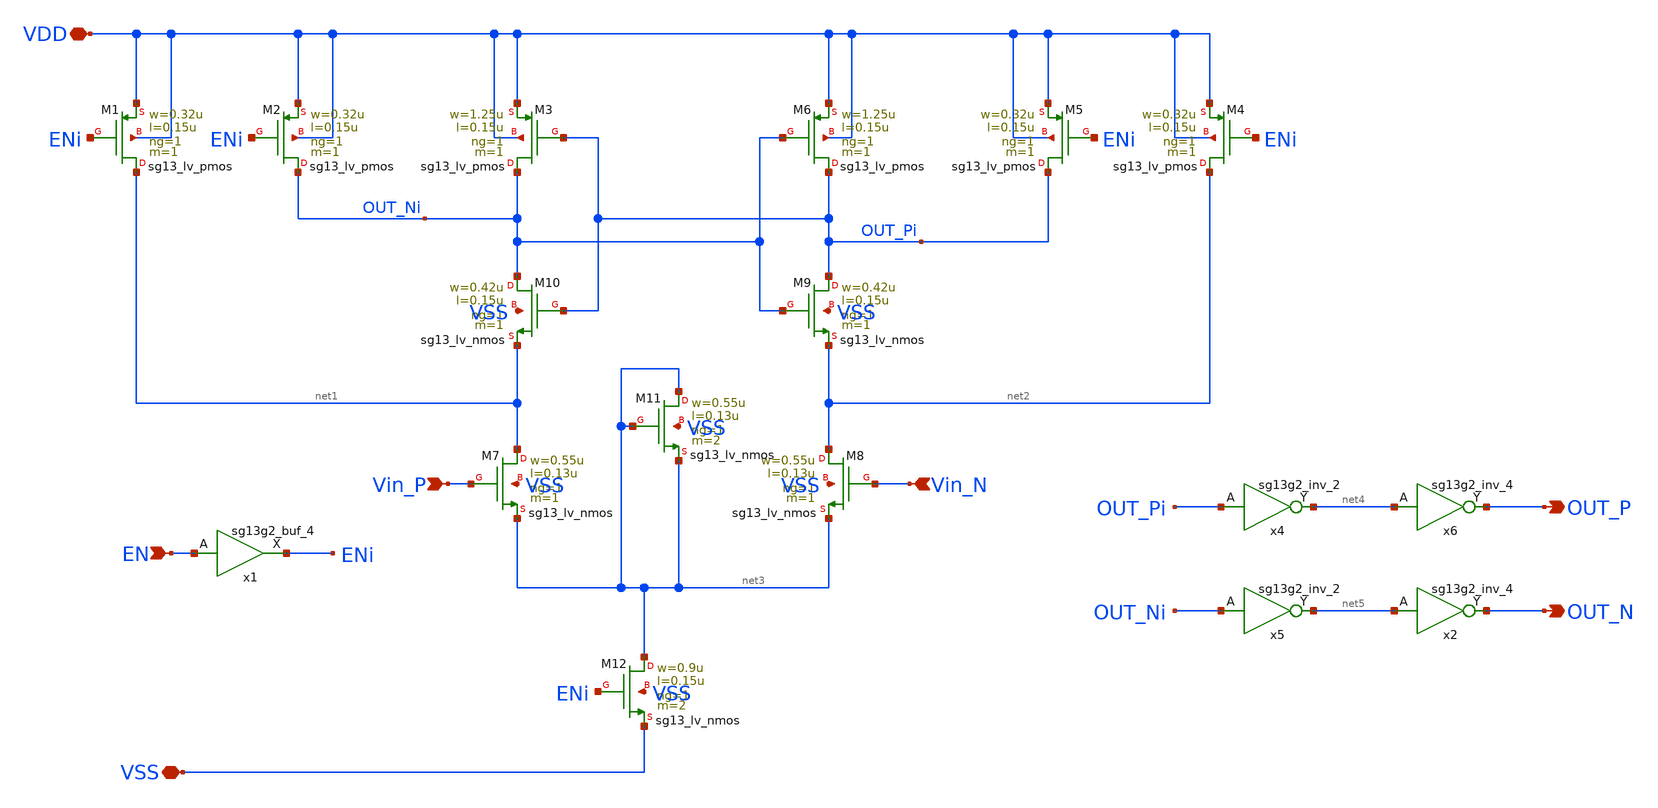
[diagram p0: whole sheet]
** sch_path: schematic/latched_comparator/latched_comparator.sch
* IHP-GmbH/IHP-Open-PDK/ihp-sg13g2/libs.tech/xschem/sg13g2_stdcells/sg13g2_buf_4.sch:
* Copyright 2023 IHP PDK Authors
* Licensed under the Apache License, Version 2.0 (the "License");
**.subckt latched_comparator Vin_P Vin_N VDD VSS EN OUT_P OUT_N
*.ipin Vin_P
*.ipin Vin_N
*.iopin VDD
*.iopin VSS
*.ipin EN
*.opin OUT_P
*.opin OUT_N
XM1 net1 ENi VDD VDD sg13_lv_pmos w=0.32u l=0.15u ng=1 m=1 mm_ok=1
XM2 OUT_Ni ENi VDD VDD sg13_lv_pmos w=0.32u l=0.15u ng=1 m=1 mm_ok=1
XM3 OUT_Ni OUT_Pi VDD VDD sg13_lv_pmos w=1.25u l=0.15u ng=1 m=1 mm_ok=1
XM4 net2 ENi VDD VDD sg13_lv_pmos w=0.32u l=0.15u ng=1 m=1 mm_ok=1
XM5 OUT_Pi ENi VDD VDD sg13_lv_pmos w=0.32u l=0.15u ng=1 m=1 mm_ok=1
XM6 OUT_Pi OUT_Ni VDD VDD sg13_lv_pmos w=1.25u l=0.15u ng=1 m=1 mm_ok=1
XM7 net1 Vin_P net3 VSS sg13_lv_nmos w=0.55u l=0.13u ng=1 m=1 mm_ok=1
XM8 net2 Vin_N net3 VSS sg13_lv_nmos w=0.55u l=0.13u ng=1 m=1 mm_ok=1
XM9 OUT_Pi OUT_Ni net2 VSS sg13_lv_nmos w=0.42u l=0.15u ng=1 m=1 mm_ok=1
XM10 OUT_Ni OUT_Pi net1 VSS sg13_lv_nmos w=0.42u l=0.15u ng=1 m=1 mm_ok=1
XM11 net3 net3 net3 VSS sg13_lv_nmos w=0.55u l=0.13u ng=1 m=2 mm_ok=1
XM12 net3 ENi VSS VSS sg13_lv_nmos w=0.9u l=0.15u ng=1 m=2 mm_ok=1
x4 net4 OUT_Pi VDD VSS sg13g2_inv_2
x5 net5 OUT_Ni VDD VSS sg13g2_inv_2
x1 ENi EN VDD VSS sg13g2_buf_4
x6 OUT_P net4 VDD VSS sg13g2_inv_4
x2 OUT_N net5 VDD VSS sg13g2_inv_4
**.ends

* expanding   symbol:  sg13g2_stdcells/sg13g2_inv_2.sym # of pins=2
** sym_path: sg13g2_stdcells/sg13g2_inv_2.sym
** sch_path: sg13g2_stdcells/sg13g2_inv_2.sch
.subckt sg13g2_inv_2 Y A VDD VSS
*.opin Y
*.ipin A
*.iopin VDD
*.iopin VSS
XM1 Y A VSS VSS sg13_lv_nmos w=1.48u l=130.00n ng=2 m=1 mm_ok=1
XM2 Y A VDD VDD sg13_lv_pmos w=2.24u l=130.00n ng=2 m=1 mm_ok=1
.ends


* expanding   symbol:  sg13g2_stdcells/sg13g2_buf_4.sym # of pins=2
** sym_path: sg13g2_stdcells/sg13g2_buf_4.sym
** sch_path: sg13g2_stdcells/sg13g2_buf_4.sch
.subckt sg13g2_buf_4 X A VDD VSS
*.ipin A
*.opin X
*.iopin VDD
*.iopin VSS
XM1 net1 A VSS VSS sg13_lv_nmos w=740.00n l=130.00n ng=1 m=1 mm_ok=1
XM2 X net1 VSS VSS sg13_lv_nmos w=2.96u l=130.00n ng=4 m=1 mm_ok=1
XM3 net1 A VDD VDD sg13_lv_pmos w=1.68u l=130.00n ng=2 m=1 mm_ok=1
XM4 X net1 VDD VDD sg13_lv_pmos w=4.48u l=130.00n ng=4 m=1 mm_ok=1
.ends


* expanding   symbol:  sg13g2_stdcells/sg13g2_inv_4.sym # of pins=2
** sym_path: sg13g2_stdcells/sg13g2_inv_4.sym
** sch_path: sg13g2_stdcells/sg13g2_inv_4.sch
.subckt sg13g2_inv_4 Y A VDD VSS
*.ipin A
*.opin Y
*.iopin VDD
*.iopin VSS
XM1 Y A VSS VSS sg13_lv_nmos w=2.96u l=130.00n ng=4 m=1 mm_ok=1
XM2 Y A VDD VDD sg13_lv_pmos w=4.48u l=130.00n ng=4 m=1 mm_ok=1
.ends

.end
